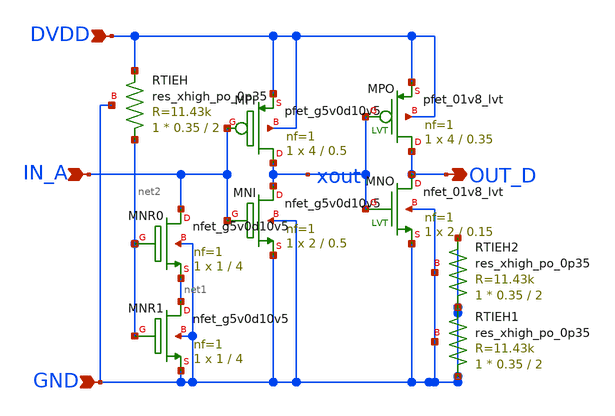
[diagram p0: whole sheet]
** sch_path: design/schematic/LVSHFTH2L_v1.sch
**.subckt LVSHFTH2L_v1 IN_A DVDD GND OUT_D
*.ipin IN_A
*.ipin DVDD
*.ipin GND
*.opin OUT_D
XMNI xout IN_A GND GND sky130_fd_pr__nfet_g5v0d10v5 L=0.5 W=2 nf=1 ad='int((1 + 1)/2) * 2 / 1 * 0.29'
+ as='int((1 + 2)/2) * 2 / 1 * 0.29' pd='2*int((1 + 1)/2) * (2 / 1 + 0.29)' ps='2*int((1 + 2)/2) * (2 / 1 + 0.29)'
+ nrd='0.29 / 2 ' nrs='0.29 / 2 ' sa=0 sb=0 sd=0 mult=1 m=1
XMPI xout IN_A DVDD DVDD sky130_fd_pr__pfet_g5v0d10v5 L=0.5 W=4 nf=1 ad='int((1 + 1)/2) * 4 / 1 * 0.29'
+ as='int((1 + 2)/2) * 4 / 1 * 0.29' pd='2*int((1 + 1)/2) * (4 / 1 + 0.29)' ps='2*int((1 + 2)/2) * (4 / 1 + 0.29)'
+ nrd='0.29 / 4 ' nrs='0.29 / 4 ' sa=0 sb=0 sd=0 mult=1 m=1
XMNR0 IN_A net2 net1 GND sky130_fd_pr__nfet_g5v0d10v5 L=4 W=1 nf=1 ad='int((1 + 1)/2) * 1 / 1 * 0.29'
+ as='int((1 + 2)/2) * 1 / 1 * 0.29' pd='2*int((1 + 1)/2) * (1 / 1 + 0.29)' ps='2*int((1 + 2)/2) * (1 / 1 + 0.29)'
+ nrd='0.29 / 1 ' nrs='0.29 / 1 ' sa=0 sb=0 sd=0 mult=1 m=1
XRTIEH net2 DVDD GND sky130_fd_pr__res_xhigh_po_0p35 L=2 mult=1 m=1
XMNR1 net1 net2 GND GND sky130_fd_pr__nfet_g5v0d10v5 L=4 W=1 nf=1 ad='int((1 + 1)/2) * 1 / 1 * 0.29'
+ as='int((1 + 2)/2) * 1 / 1 * 0.29' pd='2*int((1 + 1)/2) * (1 / 1 + 0.29)' ps='2*int((1 + 2)/2) * (1 / 1 + 0.29)'
+ nrd='0.29 / 1 ' nrs='0.29 / 1 ' sa=0 sb=0 sd=0 mult=1 m=1
XMPO OUT_D xout DVDD DVDD sky130_fd_pr__pfet_01v8_lvt L=0.35 W=4 nf=1 ad='int((nf+1)/2) * W/nf * 0.29'
+ as='int((nf+2)/2) * W/nf * 0.29' pd='2*int((nf+1)/2) * (W/nf + 0.29)' ps='2*int((nf+2)/2) * (W/nf + 0.29)'
+ nrd='0.29 / W' nrs='0.29 / W' sa=0 sb=0 sd=0 mult=1 m=1
XMNO OUT_D xout GND GND sky130_fd_pr__nfet_01v8_lvt L=0.15 W=2 nf=1 ad='int((nf+1)/2) * W/nf * 0.29'
+ as='int((nf+2)/2) * W/nf * 0.29' pd='2*int((nf+1)/2) * (W/nf + 0.29)' ps='2*int((nf+2)/2) * (W/nf + 0.29)'
+ nrd='0.29 / W' nrs='0.29 / W' sa=0 sb=0 sd=0 mult=1 m=1
XRTIEH1 GND GND GND sky130_fd_pr__res_xhigh_po_0p35 L=2 mult=1 m=1
XRTIEH2 GND GND GND sky130_fd_pr__res_xhigh_po_0p35 L=2 mult=1 m=1
**.ends
.end
